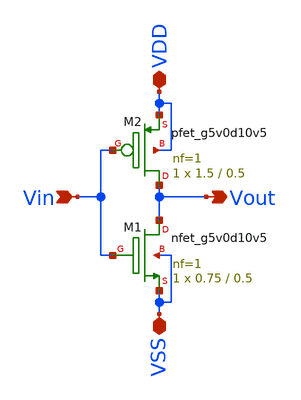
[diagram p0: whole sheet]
** sch_path: xschem/Inverter.sch
**.subckt Inverter Vin VDD VSS Vout
*.ipin Vin
*.iopin VDD
*.iopin VSS
*.opin Vout
XM1 Vout Vin VSS VSS sky130_fd_pr__nfet_g5v0d10v5 L=0.5 W=0.75 nf=1 ad='int((nf+1)/2) * W/nf * 0.29'
+ as='int((nf+2)/2) * W/nf * 0.29' pd='2*int((nf+1)/2) * (W/nf + 0.29)' ps='2*int((nf+2)/2) * (W/nf + 0.29)'
+ nrd='0.29 / W' nrs='0.29 / W' sa=0 sb=0 sd=0 mult=1 m=1
XM2 Vout Vin VDD VDD sky130_fd_pr__pfet_g5v0d10v5 L=0.5 W=1.5 nf=1 ad='int((nf+1)/2) * W/nf * 0.29' as='int((nf+2)/2) * W/nf * 0.29'
+ pd='2*int((nf+1)/2) * (W/nf + 0.29)' ps='2*int((nf+2)/2) * (W/nf + 0.29)' nrd='0.29 / W' nrs='0.29 / W'
+ sa=0 sb=0 sd=0 mult=1 m=1
**.ends
.end
